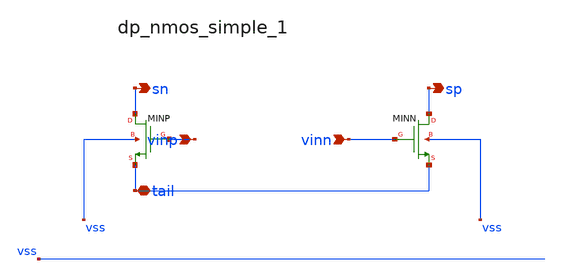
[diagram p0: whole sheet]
** sch_path: analog-db/raw/cmp_002_strongarm/hier/blocks/dp_nmos_simple_1.sch
**.subckt dp_nmos_simple_1 vinp vinn tail sn sp
*.ipin vinp
*.ipin vinn
*.iopin tail
*.opin sn
*.opin sp
XMINN sp vinn tail vss sg13_lv_nmos w=x_dut_xminn_w l=x_dut_xminn_l ng=1 m=x_dut_xminn_m
XMINP sn vinp tail vss sg13_lv_nmos w=x_dut_xminp_w l=x_dut_xminp_l ng=1 m=x_dut_xminp_m
**.ends
.end
